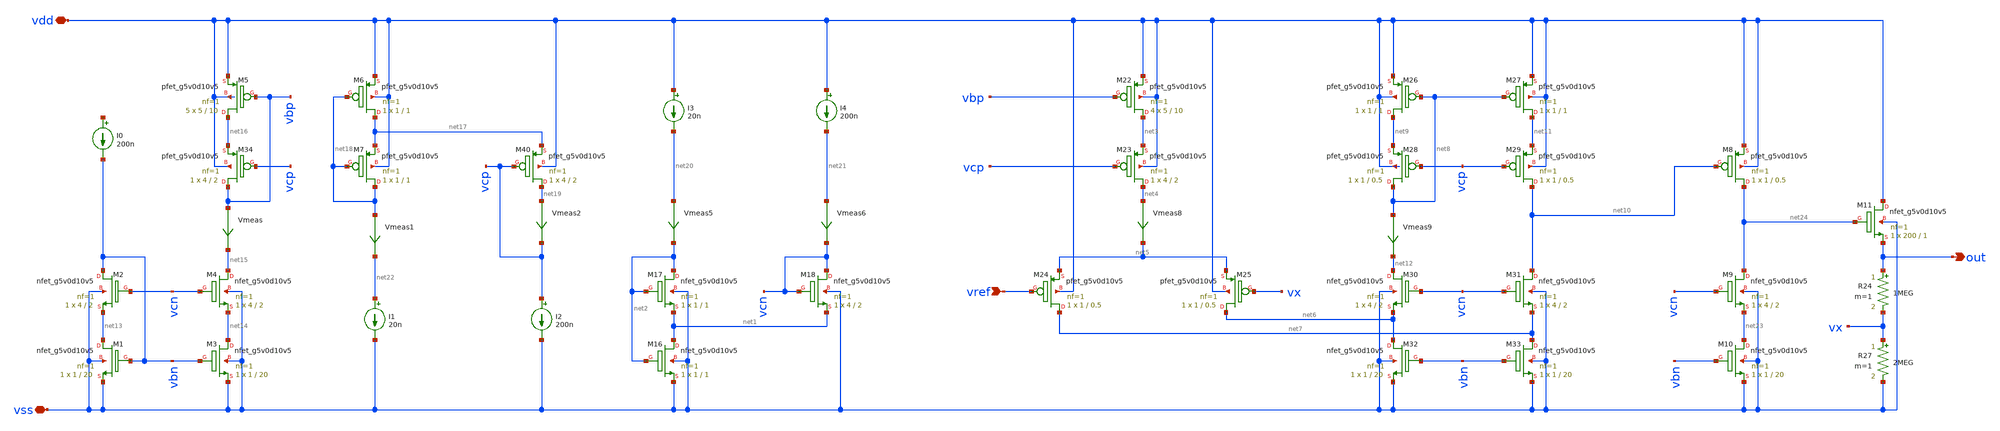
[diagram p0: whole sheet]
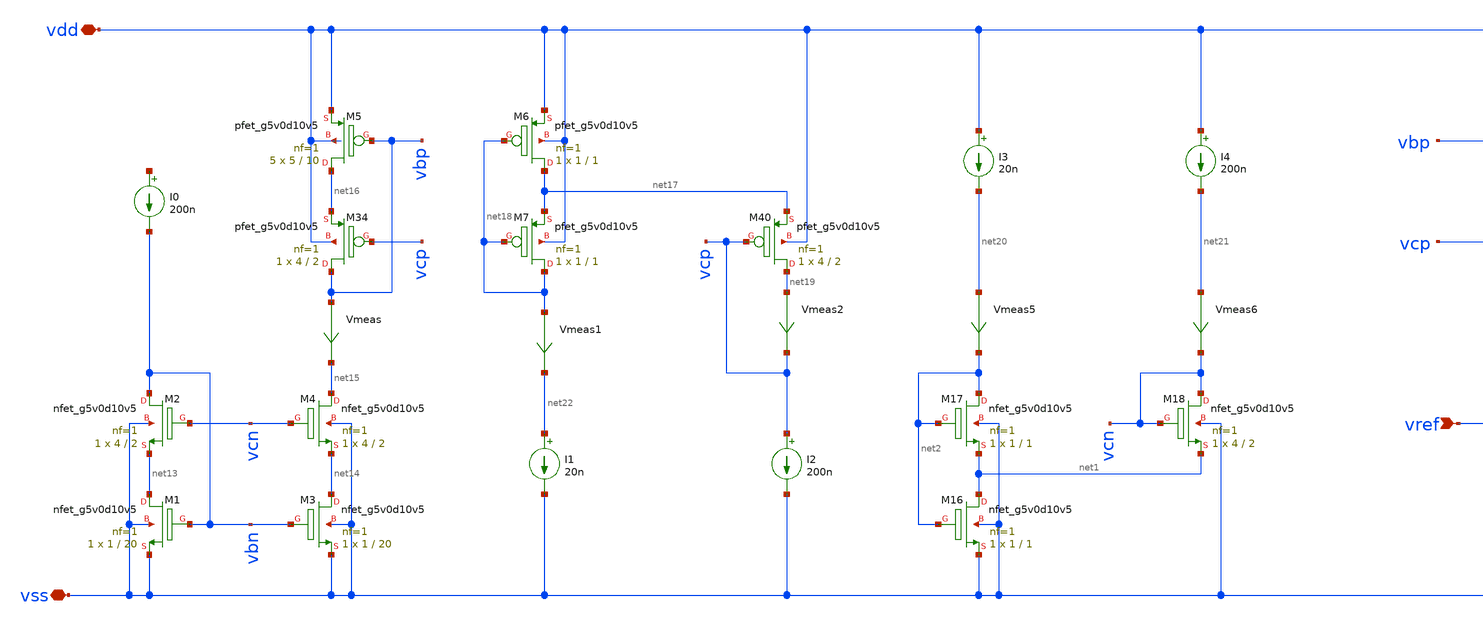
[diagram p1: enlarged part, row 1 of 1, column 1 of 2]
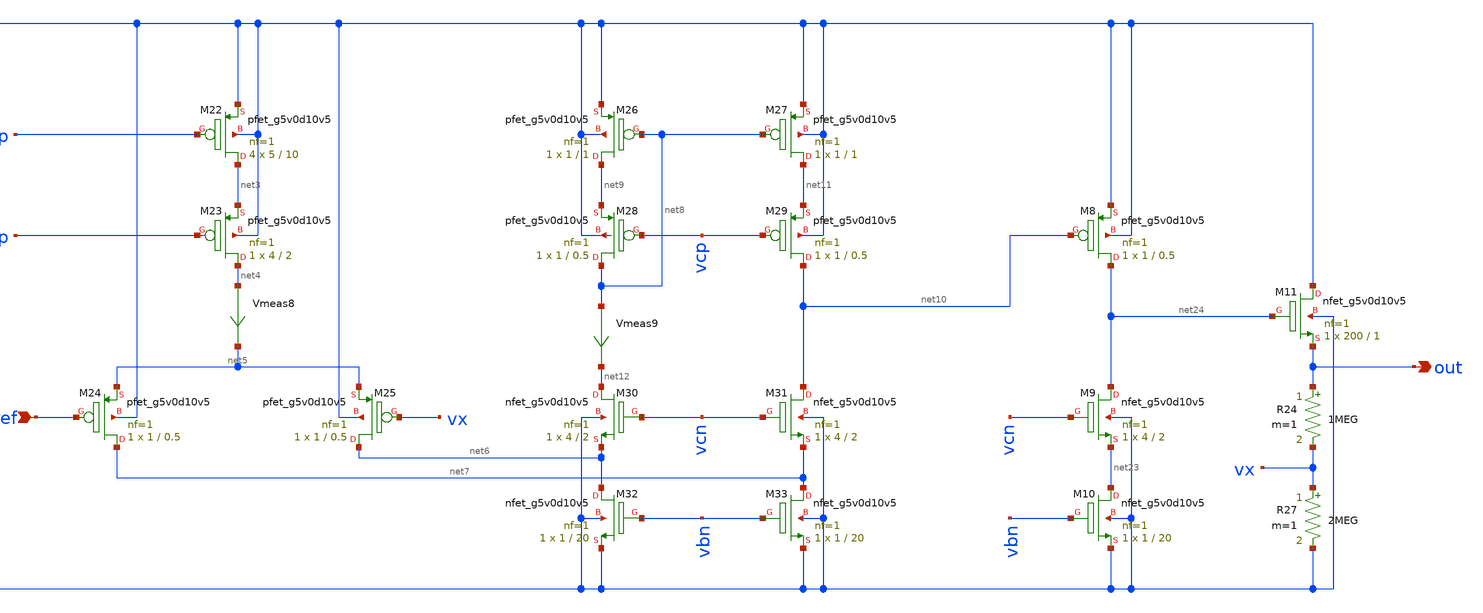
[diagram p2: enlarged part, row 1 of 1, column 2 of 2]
** sch_path: xschem/ldo.sch
**.subckt ldo out vref vdd vss
*.opin out
*.ipin vref
*.iopin vdd
*.iopin vss
XM1 net13 vbn vss vss sky130_fd_pr__nfet_g5v0d10v5 L=20 W=1 nf=1 ad='int((nf+1)/2) * W/nf * 0.29' as='int((nf+2)/2) * W/nf * 0.29'
+ pd='2*int((nf+1)/2) * (W/nf + 0.29)' ps='2*int((nf+2)/2) * (W/nf + 0.29)' nrd='0.29 / W' nrs='0.29 / W'
+ sa=0 sb=0 sd=0 mult=1 m=1
XM3 net14 vbn vss vss sky130_fd_pr__nfet_g5v0d10v5 L=20 W=1 nf=1 ad='int((nf+1)/2) * W/nf * 0.29' as='int((nf+2)/2) * W/nf * 0.29'
+ pd='2*int((nf+1)/2) * (W/nf + 0.29)' ps='2*int((nf+2)/2) * (W/nf + 0.29)' nrd='0.29 / W' nrs='0.29 / W'
+ sa=0 sb=0 sd=0 mult=1 m=1
XM5 net16 vbp vdd vdd sky130_fd_pr__pfet_g5v0d10v5 L=10 W=5 nf=1 ad='int((nf+1)/2) * W/nf * 0.29' as='int((nf+2)/2) * W/nf * 0.29'
+ pd='2*int((nf+1)/2) * (W/nf + 0.29)' ps='2*int((nf+2)/2) * (W/nf + 0.29)' nrd='0.29 / W' nrs='0.29 / W'
+ sa=0 sb=0 sd=0 mult=5 m=5
I0 net25 vbn 200n
XM16 net1 net2 vss vss sky130_fd_pr__nfet_g5v0d10v5 L=1 W=1 nf=1 ad='int((nf+1)/2) * W/nf * 0.29' as='int((nf+2)/2) * W/nf * 0.29'
+ pd='2*int((nf+1)/2) * (W/nf + 0.29)' ps='2*int((nf+2)/2) * (W/nf + 0.29)' nrd='0.29 / W' nrs='0.29 / W'
+ sa=0 sb=0 sd=0 mult=1 m=1
XM17 net2 net2 net1 vss sky130_fd_pr__nfet_g5v0d10v5 L=1 W=1 nf=1 ad='int((nf+1)/2) * W/nf * 0.29' as='int((nf+2)/2) * W/nf * 0.29'
+ pd='2*int((nf+1)/2) * (W/nf + 0.29)' ps='2*int((nf+2)/2) * (W/nf + 0.29)' nrd='0.29 / W' nrs='0.29 / W'
+ sa=0 sb=0 sd=0 mult=1 m=1
XM18 vcn vcn net1 vss sky130_fd_pr__nfet_g5v0d10v5 L=2 W=4 nf=1 ad='int((nf+1)/2) * W/nf * 0.29' as='int((nf+2)/2) * W/nf * 0.29'
+ pd='2*int((nf+1)/2) * (W/nf + 0.29)' ps='2*int((nf+2)/2) * (W/nf + 0.29)' nrd='0.29 / W' nrs='0.29 / W'
+ sa=0 sb=0 sd=0 mult=1 m=1
Vmeas vbp net15 0
.save i(vmeas)
Vmeas5 net20 net2 0
.save i(vmeas5)
Vmeas6 net21 vcn 0
.save i(vmeas6)
XM22 net3 vbp vdd vdd sky130_fd_pr__pfet_g5v0d10v5 L=10 W=5 nf=1 ad='int((nf+1)/2) * W/nf * 0.29' as='int((nf+2)/2) * W/nf * 0.29'
+ pd='2*int((nf+1)/2) * (W/nf + 0.29)' ps='2*int((nf+2)/2) * (W/nf + 0.29)' nrd='0.29 / W' nrs='0.29 / W'
+ sa=0 sb=0 sd=0 mult=4 m=4
XM23 net4 vcp net3 vdd sky130_fd_pr__pfet_g5v0d10v5 L=2 W=4 nf=1 ad='int((nf+1)/2) * W/nf * 0.29' as='int((nf+2)/2) * W/nf * 0.29'
+ pd='2*int((nf+1)/2) * (W/nf + 0.29)' ps='2*int((nf+2)/2) * (W/nf + 0.29)' nrd='0.29 / W' nrs='0.29 / W'
+ sa=0 sb=0 sd=0 mult=1 m=1
Vmeas8 net4 net5 0
.save i(vmeas8)
XM24 net7 vref net5 vdd sky130_fd_pr__pfet_g5v0d10v5 L=0.5 W=1 nf=1 ad='int((nf+1)/2) * W/nf * 0.29'
+ as='int((nf+2)/2) * W/nf * 0.29' pd='2*int((nf+1)/2) * (W/nf + 0.29)' ps='2*int((nf+2)/2) * (W/nf + 0.29)'
+ nrd='0.29 / W' nrs='0.29 / W' sa=0 sb=0 sd=0 mult=1 m=1
XM25 net6 vx net5 vdd sky130_fd_pr__pfet_g5v0d10v5 L=0.5 W=1 nf=1 ad='int((nf+1)/2) * W/nf * 0.29' as='int((nf+2)/2) * W/nf * 0.29'
+ pd='2*int((nf+1)/2) * (W/nf + 0.29)' ps='2*int((nf+2)/2) * (W/nf + 0.29)' nrd='0.29 / W' nrs='0.29 / W'
+ sa=0 sb=0 sd=0 mult=1 m=1
XM26 net9 net8 vdd vdd sky130_fd_pr__pfet_g5v0d10v5 L=1 W=1 nf=1 ad='int((nf+1)/2) * W/nf * 0.29' as='int((nf+2)/2) * W/nf * 0.29'
+ pd='2*int((nf+1)/2) * (W/nf + 0.29)' ps='2*int((nf+2)/2) * (W/nf + 0.29)' nrd='0.29 / W' nrs='0.29 / W'
+ sa=0 sb=0 sd=0 mult=1 m=1
XM27 net11 net8 vdd vdd sky130_fd_pr__pfet_g5v0d10v5 L=1 W=1 nf=1 ad='int((nf+1)/2) * W/nf * 0.29' as='int((nf+2)/2) * W/nf * 0.29'
+ pd='2*int((nf+1)/2) * (W/nf + 0.29)' ps='2*int((nf+2)/2) * (W/nf + 0.29)' nrd='0.29 / W' nrs='0.29 / W'
+ sa=0 sb=0 sd=0 mult=1 m=1
XM28 net8 vcp net9 vdd sky130_fd_pr__pfet_g5v0d10v5 L=0.5 W=1 nf=1 ad='int((nf+1)/2) * W/nf * 0.29' as='int((nf+2)/2) * W/nf * 0.29'
+ pd='2*int((nf+1)/2) * (W/nf + 0.29)' ps='2*int((nf+2)/2) * (W/nf + 0.29)' nrd='0.29 / W' nrs='0.29 / W'
+ sa=0 sb=0 sd=0 mult=1 m=1
XM29 net10 vcp net11 vdd sky130_fd_pr__pfet_g5v0d10v5 L=0.5 W=1 nf=1 ad='int((nf+1)/2) * W/nf * 0.29'
+ as='int((nf+2)/2) * W/nf * 0.29' pd='2*int((nf+1)/2) * (W/nf + 0.29)' ps='2*int((nf+2)/2) * (W/nf + 0.29)'
+ nrd='0.29 / W' nrs='0.29 / W' sa=0 sb=0 sd=0 mult=1 m=1
XM30 net12 vcn net6 vss sky130_fd_pr__nfet_g5v0d10v5 L=2 W=4 nf=1 ad='int((nf+1)/2) * W/nf * 0.29' as='int((nf+2)/2) * W/nf * 0.29'
+ pd='2*int((nf+1)/2) * (W/nf + 0.29)' ps='2*int((nf+2)/2) * (W/nf + 0.29)' nrd='0.29 / W' nrs='0.29 / W'
+ sa=0 sb=0 sd=0 mult=1 m=1
XM31 net10 vcn net7 vss sky130_fd_pr__nfet_g5v0d10v5 L=2 W=4 nf=1 ad='int((nf+1)/2) * W/nf * 0.29' as='int((nf+2)/2) * W/nf * 0.29'
+ pd='2*int((nf+1)/2) * (W/nf + 0.29)' ps='2*int((nf+2)/2) * (W/nf + 0.29)' nrd='0.29 / W' nrs='0.29 / W'
+ sa=0 sb=0 sd=0 mult=1 m=1
XM32 net6 vbn vss vss sky130_fd_pr__nfet_g5v0d10v5 L=20 W=1 nf=1 ad='int((nf+1)/2) * W/nf * 0.29' as='int((nf+2)/2) * W/nf * 0.29'
+ pd='2*int((nf+1)/2) * (W/nf + 0.29)' ps='2*int((nf+2)/2) * (W/nf + 0.29)' nrd='0.29 / W' nrs='0.29 / W'
+ sa=0 sb=0 sd=0 mult=1 m=1
XM33 net7 vbn vss vss sky130_fd_pr__nfet_g5v0d10v5 L=20 W=1 nf=1 ad='int((nf+1)/2) * W/nf * 0.29' as='int((nf+2)/2) * W/nf * 0.29'
+ pd='2*int((nf+1)/2) * (W/nf + 0.29)' ps='2*int((nf+2)/2) * (W/nf + 0.29)' nrd='0.29 / W' nrs='0.29 / W'
+ sa=0 sb=0 sd=0 mult=1 m=1
Vmeas9 net8 net12 0
.save i(vmeas9)
XM2 vbn vcn net13 vss sky130_fd_pr__nfet_g5v0d10v5 L=2 W=4 nf=1 ad='int((nf+1)/2) * W/nf * 0.29' as='int((nf+2)/2) * W/nf * 0.29'
+ pd='2*int((nf+1)/2) * (W/nf + 0.29)' ps='2*int((nf+2)/2) * (W/nf + 0.29)' nrd='0.29 / W' nrs='0.29 / W'
+ sa=0 sb=0 sd=0 mult=1 m=1
XM4 net15 vcn net14 vss sky130_fd_pr__nfet_g5v0d10v5 L=2 W=4 nf=1 ad='int((nf+1)/2) * W/nf * 0.29' as='int((nf+2)/2) * W/nf * 0.29'
+ pd='2*int((nf+1)/2) * (W/nf + 0.29)' ps='2*int((nf+2)/2) * (W/nf + 0.29)' nrd='0.29 / W' nrs='0.29 / W'
+ sa=0 sb=0 sd=0 mult=1 m=1
XM34 vbp vcp net16 vdd sky130_fd_pr__pfet_g5v0d10v5 L=2 W=4 nf=1 ad='int((nf+1)/2) * W/nf * 0.29' as='int((nf+2)/2) * W/nf * 0.29'
+ pd='2*int((nf+1)/2) * (W/nf + 0.29)' ps='2*int((nf+2)/2) * (W/nf + 0.29)' nrd='0.29 / W' nrs='0.29 / W'
+ sa=0 sb=0 sd=0 mult=1 m=1
XM6 net17 net18 vdd vdd sky130_fd_pr__pfet_g5v0d10v5 L=1 W=1 nf=1 ad='int((nf+1)/2) * W/nf * 0.29' as='int((nf+2)/2) * W/nf * 0.29'
+ pd='2*int((nf+1)/2) * (W/nf + 0.29)' ps='2*int((nf+2)/2) * (W/nf + 0.29)' nrd='0.29 / W' nrs='0.29 / W'
+ sa=0 sb=0 sd=0 mult=1 m=1
XM7 net18 net18 net17 vdd sky130_fd_pr__pfet_g5v0d10v5 L=1 W=1 nf=1 ad='int((nf+1)/2) * W/nf * 0.29'
+ as='int((nf+2)/2) * W/nf * 0.29' pd='2*int((nf+1)/2) * (W/nf + 0.29)' ps='2*int((nf+2)/2) * (W/nf + 0.29)'
+ nrd='0.29 / W' nrs='0.29 / W' sa=0 sb=0 sd=0 mult=1 m=1
Vmeas1 net18 net22 0
.save i(vmeas1)
XM40 net19 vcp net17 vdd sky130_fd_pr__pfet_g5v0d10v5 L=2 W=4 nf=1 ad='int((nf+1)/2) * W/nf * 0.29' as='int((nf+2)/2) * W/nf * 0.29'
+ pd='2*int((nf+1)/2) * (W/nf + 0.29)' ps='2*int((nf+2)/2) * (W/nf + 0.29)' nrd='0.29 / W' nrs='0.29 / W'
+ sa=0 sb=0 sd=0 mult=1 m=1
Vmeas2 net19 vcp 0
.save i(vmeas2)
I1 net22 vss 20n
I2 vcp vss 200n
I3 vdd net20 20n
I4 vdd net21 200n
XM8 net24 net10 vdd vdd sky130_fd_pr__pfet_g5v0d10v5 L=0.5 W=1 nf=1 ad='int((nf+1)/2) * W/nf * 0.29'
+ as='int((nf+2)/2) * W/nf * 0.29' pd='2*int((nf+1)/2) * (W/nf + 0.29)' ps='2*int((nf+2)/2) * (W/nf + 0.29)'
+ nrd='0.29 / W' nrs='0.29 / W' sa=0 sb=0 sd=0 mult=1 m=1
XM9 net24 vcn net23 vss sky130_fd_pr__nfet_g5v0d10v5 L=2 W=4 nf=1 ad='int((nf+1)/2) * W/nf * 0.29' as='int((nf+2)/2) * W/nf * 0.29'
+ pd='2*int((nf+1)/2) * (W/nf + 0.29)' ps='2*int((nf+2)/2) * (W/nf + 0.29)' nrd='0.29 / W' nrs='0.29 / W'
+ sa=0 sb=0 sd=0 mult=1 m=1
XM10 net23 vbn vss vss sky130_fd_pr__nfet_g5v0d10v5 L=20 W=1 nf=1 ad='int((nf+1)/2) * W/nf * 0.29' as='int((nf+2)/2) * W/nf * 0.29'
+ pd='2*int((nf+1)/2) * (W/nf + 0.29)' ps='2*int((nf+2)/2) * (W/nf + 0.29)' nrd='0.29 / W' nrs='0.29 / W'
+ sa=0 sb=0 sd=0 mult=1 m=1
XM11 vdd net24 out vss sky130_fd_pr__nfet_g5v0d10v5 L=1 W=200 nf=1 ad='int((nf+1)/2) * W/nf * 0.29' as='int((nf+2)/2) * W/nf * 0.29'
+ pd='2*int((nf+1)/2) * (W/nf + 0.29)' ps='2*int((nf+2)/2) * (W/nf + 0.29)' nrd='0.29 / W' nrs='0.29 / W'
+ sa=0 sb=0 sd=0 mult=1 m=1
R24 out vx 1MEG m=1
R27 vx vss 2MEG m=1
**** begin user architecture code

vref vref 0 1.2
vss vss 0 0
vdd vdd 0 3.3 ac 1
.option savecurrents
.control
save all
save @m.xm25.msky130_fd_pr__pfet_g5v0d10v5[gm]
save @m.xm25.msky130_fd_pr__pfet_g5v0d10v5[gds]
save @m.xm27.msky130_fd_pr__pfet_g5v0d10v5[gm]
save @m.xm27.msky130_fd_pr__pfet_g5v0d10v5[gds]
save @m.xm29.msky130_fd_pr__pfet_g5v0d10v5[gm]
save @m.xm29.msky130_fd_pr__pfet_g5v0d10v5[gds]
save @m.xm31.msky130_fd_pr__nfet_g5v0d10v5[gm]
save @m.xm31.msky130_fd_pr__nfet_g5v0d10v5[gds]
save @m.xm4.msky130_fd_pr__nfet_g5v0d10v5[gm]
save @m.xm4.msky130_fd_pr__nfet_g5v0d10v5[gds]
save @m.xm33.msky130_fd_pr__nfet_g5v0d10v5[gm]
save @m.xm33.msky130_fd_pr__nfet_g5v0d10v5[id]
save @m.xm33.msky130_fd_pr__nfet_g5v0d10v5[gds]
save @m.xm3.msky130_fd_pr__nfet_g5v0d10v5[gds]
save @m.xm1.msky130_fd_pr__nfet_g5v0d10v5[gds]
save @m.xm9.msky130_fd_pr__nfet_g5v0d10v5[id]
op
write bias_generator.raw
set appendwrite
* quit
* === analysis ===
ac dec 10 10 10MEG
write bias_generator.raw
set units=degrees
plot db(out)
plot ph(out)
.endc


.lib $::SKYWATER_MODELS/sky130.lib.spice tt
**** end user architecture code
**.ends
.end
